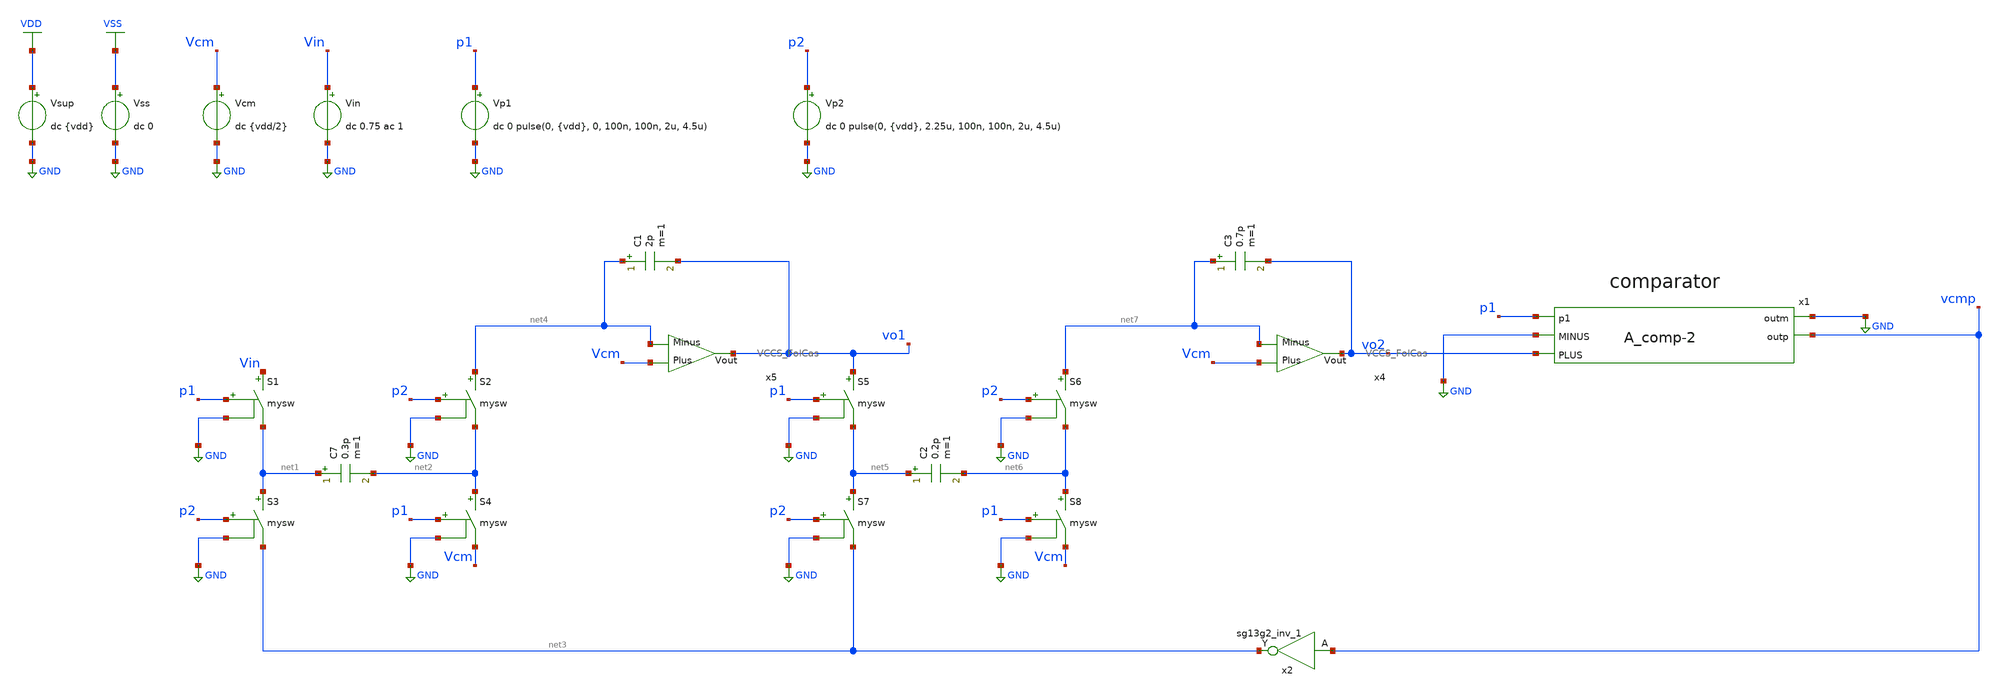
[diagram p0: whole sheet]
** sch_path: DSM/Schematics/IC_Designs_Hrishi/RealCircuits/Real_DSM (2).sch
**.subckt Real_DSM (2)
Vcm Vcm GND dc {vdd/2}
Vin Vin GND dc 0.75 ac 1
S1 Vin net1 p1 GND mysw
S2 net4 net2 p2 GND mysw
S3 net1 net3 p2 GND mysw
S4 net2 Vcm p1 GND mysw
C7 net1 net2 0.3p m=1
C1 net4 vo1 2p m=1
S5 vo1 net5 p1 GND mysw
S6 net7 net6 p2 GND mysw
S7 net5 net3 p2 GND mysw
S8 net6 Vcm p1 GND mysw
C2 net5 net6 0.2p m=1
C3 net7 vo2 0.7p m=1
x2 net3 vcmp Vdd Vss sg13g2_inv_1
Vsup VDD GND dc {vdd}
Vss VSS GND dc 0
x5 Vcm vo1 net4 VCCS_FolCas
x4 Vcm vo2 net7 VCCS_FolCas
Vp1 p1 GND dc 0 pulse(0, {vdd}, 0, 100n, 100n, 2u, 4.5u)
Vp2 p2 GND dc 0 pulse(0, {vdd}, 2.25u, 100n, 100n, 2u, 4.5u)
x1 p1 GND vcmp GND vo2 A_comp-2
**** begin user architecture code

.lib $::SG13G2_MODELS/cornerMOSlv.lib mos_tt
.lib $::SG13G2_MODELS/cornerRES.lib res_typ
.inc /foss/pdks/sg13g2/libs.ref/sg13g2_stdcell/spice/sg13g2_stdcell.spice



.param temp=27 vdd = 1.5
.model mysw SW vt={vdd/2} ron=0.1
.option method=gear reltol=1e-4

.control
save all
run
tran 0.45m 0.45m
plot vo1 vo2 vcmp

set wr_singlescale
set wr_vecnames
wrdata IDEAL_SwitchCap.txt vo1 vo2 vcmp p1 p2
.endc


**** end user architecture code
**.ends
.GLOBAL GND
.GLOBAL VDD
.GLOBAL VSS
.end
